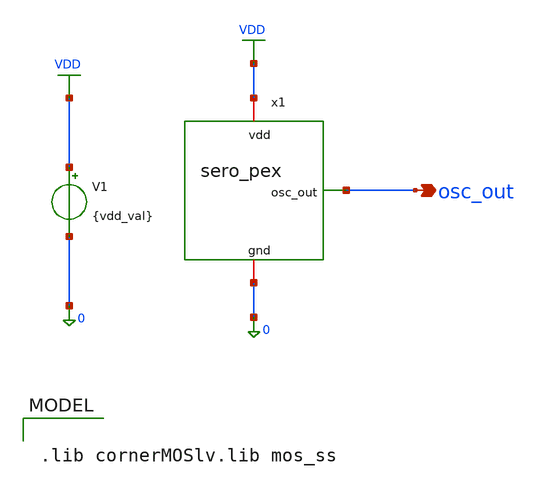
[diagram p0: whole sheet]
** sch_path: simulations/tb/vdd_v_freq_pex.sch
**.subckt vdd_v_freq_pex osc_out
*.opin osc_out
x1 VDD osc_out 0 sero_pex
V1 VDD 0 {vdd_val}
**** begin user architecture code

.lib cornerMOSlv.lib mos_ss



.param vdd_val=1.2
.ic v(osc_out) 0
.control
  save all
  let v_start = 0.96
  let v_stop  = 1.44
  let v_step  = 0.06
  let n_pts   = 9
  let vdds  = vector(n_pts)
  let freqs = vector(n_pts)
  let powers = vector(n_pts)
  let idx = 0

  while idx < n_pts
    let v_curr = v_start + idx * v_step
    alterparam vdd_val = $&v_curr
    reset

    * --- Pilot run: rough period estimate ---
    tran 5p 14n
    meas tran tp1 when v(osc_out)=0.5*v_curr rise=2 td=7n
    meas tran tp2 when v(osc_out)=0.5*v_curr rise=3 td=7n
    let period_est = tp2 - tp1
    let tstop_v     = 15 * period_est + 8n
    let ifrom_v     = period_est * 8
    let ito_v       = period_est * 12

    * --- capture as plain control-level scalars BEFORE any further reset ---
    set tstop_s = $&tstop_v
    set ifrom_s = $&ifrom_v
    set ito_s   = $&ito_v

    * --- Re-run sized for settled oscillation ---
    reset
    alterparam vdd_val = $&v_curr
    reset
    tran 2p $tstop_s

    meas tran t1 when v(osc_out)=0.5*v_curr rise=9  td=5n
    meas tran t2 when v(osc_out)=0.5*v_curr rise=10 td=5n
    meas tran iavg avg i(v1) from=$ifrom_s to=$ito_s

    let freqs[idx]  = 1 / (t2 - t1)
    let powers[idx] = -iavg * v_curr
    let vdds[idx]   = v_curr
    let idx = idx + 1
  end

  set curplot = control
  write vdd_v_freq_pex.raw freqs vdds powers
.endc

**** end user architecture code
**.ends

* expanding   symbol:  /foss/designs/sero/design/symbol/sero_pex.sym # of pins=3
** sym_path: design/symbol/sero.sym
.include /foss/designs/sero/simulations/pex/sero_lyt.pex.spice
.GLOBAL VDD
.end
